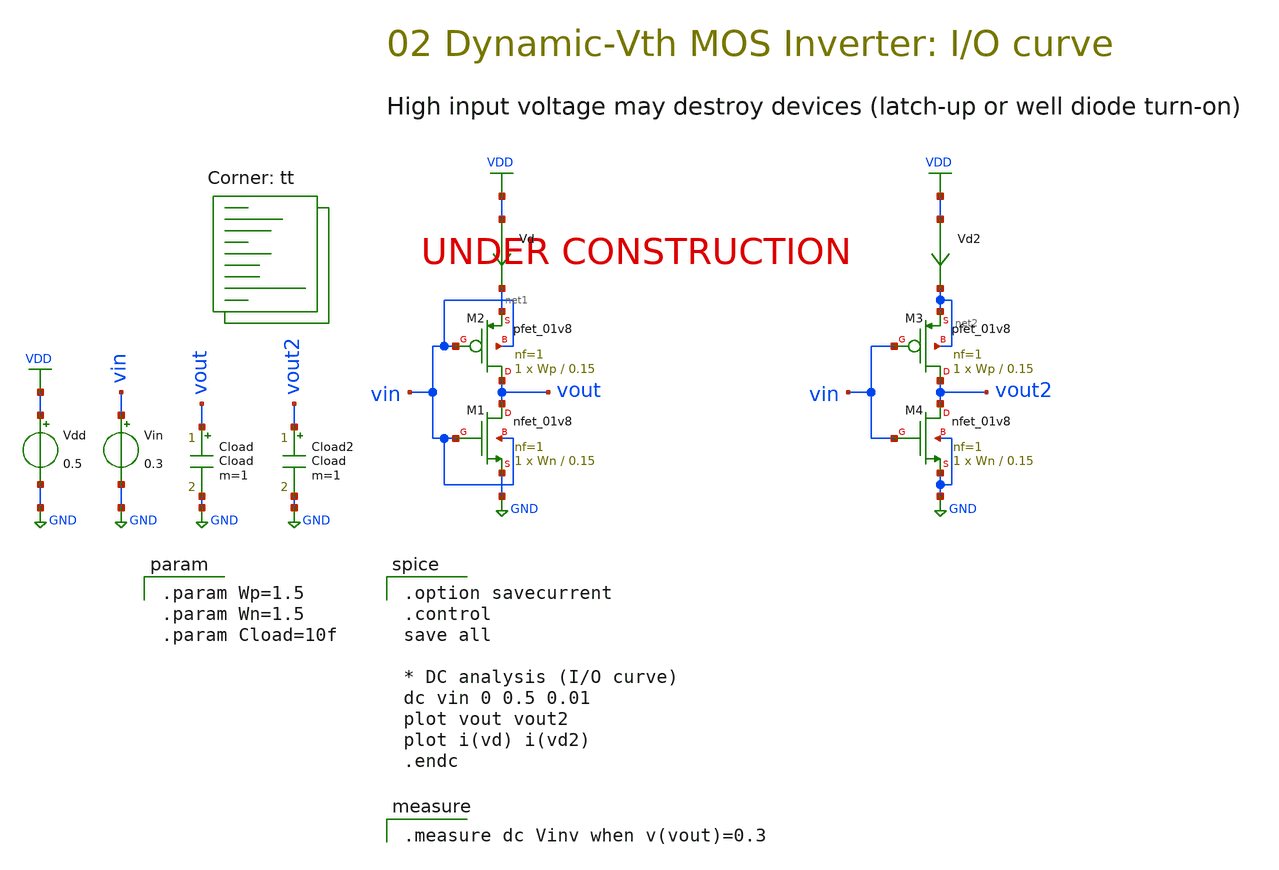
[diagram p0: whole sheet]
** sch_path: 02-a_dtmos.sch
**.subckt 02-a_dtmos
Vdd VDD GND 0.5
Vin vin GND 0.3
Vd VDD net1 0
.save i(vd)
XM3 vout2 vin net2 net2 sky130_fd_pr__pfet_01v8 L=0.15 W=Wp nf=1 ad='int((nf+1)/2) * W/nf * 0.29' as='int((nf+2)/2) * W/nf * 0.29'
+ pd='2*int((nf+1)/2) * (W/nf + 0.29)' ps='2*int((nf+2)/2) * (W/nf + 0.29)' nrd='0.29 / W' nrs='0.29 / W'
+ sa=0 sb=0 sd=0 mult=1 m=1
XM4 vout2 vin GND GND sky130_fd_pr__nfet_01v8 L=0.15 W=Wn nf=1 ad='int((1 + 1)/2) * Wn / 1 * 0.29' as='int((1 + 2)/2) * Wn / 1 * 0.29'
+ pd='2*int((1 + 1)/2) * (Wn / 1 + 0.29)' ps='2*int((1 + 2)/2) * (Wn / 1 + 0.29)' nrd='0.29 / Wn ' nrs='0.29 / Wn '
+ sa=0 sb=0 sd=0 mult=1 m=1
Vd2 VDD net2 0
.save i(vd2)
XM1 vout vin GND vin sky130_fd_pr__nfet_01v8 L=0.15 W=Wn nf=1 ad='int((1 + 1)/2) * Wn / 1 * 0.29' as='int((1 + 2)/2) * Wn / 1 * 0.29'
+ pd='2*int((1 + 1)/2) * (Wn / 1 + 0.29)' ps='2*int((1 + 2)/2) * (Wn / 1 + 0.29)' nrd='0.29 / Wn ' nrs='0.29 / Wn '
+ sa=0 sb=0 sd=0 mult=1 m=1
XM2 vout vin net1 vin sky130_fd_pr__pfet_01v8 L=0.15 W=Wp nf=1 ad='int((nf+1)/2) * W/nf * 0.29' as='int((nf+2)/2) * W/nf * 0.29'
+ pd='2*int((nf+1)/2) * (W/nf + 0.29)' ps='2*int((nf+2)/2) * (W/nf + 0.29)' nrd='0.29 / W' nrs='0.29 / W'
+ sa=0 sb=0 sd=0 mult=1 m=1
Cload vout GND Cload m=1
Cload2 vout2 GND Cload m=1
**** begin user architecture code
.lib $::SKYWATER_MODELS/sky130.lib.spice tt

.param Wp=1.5
.param Wn=1.5
.param Cload=10f


.option savecurrent
.control
save all

* DC analysis (I/O curve)
dc vin 0 0.5 0.01
plot vout vout2
plot i(vd) i(vd2)
.endc


.measure dc Vinv when v(vout)=0.3

**** end user architecture code
**.ends
.GLOBAL GND
.GLOBAL VDD
.end
